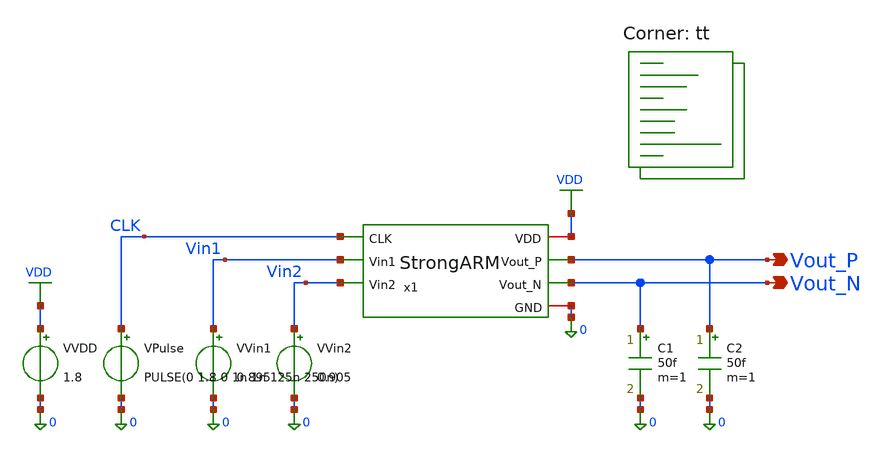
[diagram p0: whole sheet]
** sch_path: blocks/03_StrongARM/sim/tb_StrongARM_Power.sch
**.subckt tb_StrongARM_Power Vout_P Vout_N
*.opin Vout_P
*.opin Vout_N
x1 VDD CLK Vout_P Vout_N Vin1 Vin2 0 StrongARM
VVDD VDD 0 1.8
VVin1 Vin1 0 0.895
VVin2 Vin2 0 0.905
VPulse CLK 0 PULSE(0 1.8 0 1n 1n 125n 250n)
C1 Vout_N 0 50f m=1
C2 Vout_P 0 50f m=1
**** begin user architecture code



.control
save all

* ============================================
* BLOCK 3 - STRONGARM COMPARATOR
* TEST 7C - FINAL OUTPUT LOADING
* SKY130 TT / VDD 1.8V / CLK 4MHz
* BOTH INPUT POLARITIES
* ============================================

echo ============================================
echo TEST 7C - FINAL CHARACTERIZATION
echo ============================================

* ============================================
* CASE A: Vin1 < Vin2
* Vout_N should FALL
* Vout_P should remain HIGH
* ============================================

alter VVin1 0.895
alter VVin2 0.905

echo CASE A - NEGATIVE DIFFERENTIAL INPUT

tran 0.05n 2.5u

meas tran delay_A TRIG v(clk) VAL=0.9 RISE=9 TARG v(vout_n) VAL=0.9 FALL=9

meas tran vp_eval_A FIND v(vout_p) AT=2.01u
meas tran vn_eval_A FIND v(vout_n) AT=2.01u

meas tran vp_reset_A FIND v(vout_p) AT=2.20u
meas tran vn_reset_A FIND v(vout_n) AT=2.20u

meas tran vp_droop_A MIN v(vout_p) FROM=2u TO=2.01u

meas tran vp_max_A MAX v(vout_p) FROM=500n TO=2.5u
meas tran vn_max_A MAX v(vout_n) FROM=500n TO=2.5u

meas tran vp_min_A MIN v(vout_p) FROM=500n TO=2.5u
meas tran vn_min_A MIN v(vout_n) FROM=500n TO=2.5u

meas tran ivdd_A AVG i(VVDD) FROM=500n TO=2.5u

let power_A_uW = -1.8 * ivdd_A * 1e6
let energy_A_pJ = power_A_uW / 4
let delay_A_ns = delay_A * 1e9

echo CASE A SUMMARY
print power_A_uW
print energy_A_pJ
print delay_A_ns

* ============================================
* CASE B: Vin1 > Vin2
* Vout_P should FALL
* Vout_N should remain HIGH
* ============================================

alter VVin1 0.905
alter VVin2 0.895

echo CASE B - POSITIVE DIFFERENTIAL INPUT

tran 0.05n 2.5u

meas tran delay_B TRIG v(clk) VAL=0.9 RISE=9 TARG v(vout_p) VAL=0.9 FALL=9

meas tran vp_eval_B FIND v(vout_p) AT=2.01u
meas tran vn_eval_B FIND v(vout_n) AT=2.01u

meas tran vp_reset_B FIND v(vout_p) AT=2.20u
meas tran vn_reset_B FIND v(vout_n) AT=2.20u

meas tran vn_droop_B MIN v(vout_n) FROM=2u TO=2.01u

meas tran vp_max_B MAX v(vout_p) FROM=500n TO=2.5u
meas tran vn_max_B MAX v(vout_n) FROM=500n TO=2.5u

meas tran vp_min_B MIN v(vout_p) FROM=500n TO=2.5u
meas tran vn_min_B MIN v(vout_n) FROM=500n TO=2.5u

meas tran ivdd_B AVG i(VVDD) FROM=500n TO=2.5u

let power_B_uW = -1.8 * ivdd_B * 1e6
let energy_B_pJ = power_B_uW / 4
let delay_B_ns = delay_B * 1e9

echo CASE B SUMMARY
print power_B_uW
print energy_B_pJ
print delay_B_ns

echo ============================================
echo BOTH POLARITIES COMPLETED
echo ============================================

.endc

.lib $::SKYWATER_MODELS/sky130.lib.spice tt
**** end user architecture code
**.ends

* expanding   symbol:  blocks/03_StrongARM/xschem/StrongARM.sym # of pins=7
** sym_path: blocks/03_StrongARM/xschem/StrongARM.sym
** sch_path: blocks/03_StrongARM/xschem/StrongARM.sch
.subckt StrongARM VDD CLK Vout_P Vout_N Vin1 Vin2 GND
*.iopin VDD
*.iopin GND
*.ipin Vin1
*.ipin Vin2
*.ipin CLK
*.opin Vout_P
*.opin Vout_N
XS1 P CLK VDD VDD sky130_fd_pr__pfet_01v8 L=0.15 W=1.5 nf=1 ad='int((1 + 1)/2) * 1.5 / 1 * 0.29' as='int((1 + 2)/2) * 1.5 / 1 * 0.29'
+ pd='2*int((1 + 1)/2) * (1.5 / 1 + 0.29)' ps='2*int((1 + 2)/2) * (1.5 / 1 + 0.29)' nrd='0.29 / 1.5 ' nrs='0.29 / 1.5 '
+ sa=0 sb=0 sd=0 mult=1 m=1
XS3 Vout_P CLK VDD VDD sky130_fd_pr__pfet_01v8 L=0.15 W=1.5 nf=1 ad='int((1 + 1)/2) * 1.5 / 1 * 0.29'
+ as='int((1 + 2)/2) * 1.5 / 1 * 0.29' pd='2*int((1 + 1)/2) * (1.5 / 1 + 0.29)' ps='2*int((1 + 2)/2) * (1.5 / 1 + 0.29)'
+ nrd='0.29 / 1.5 ' nrs='0.29 / 1.5 ' sa=0 sb=0 sd=0 mult=1 m=1
XM5 Vout_P Vout_N VDD VDD sky130_fd_pr__pfet_01v8 L=0.3 W=5 nf=1 ad='int((1 + 1)/2) * 5 / 1 * 0.29' as='int((1 + 2)/2) * 5 / 1 * 0.29'
+ pd='2*int((1 + 1)/2) * (5 / 1 + 0.29)' ps='2*int((1 + 2)/2) * (5 / 1 + 0.29)' nrd='0.29 / 5 ' nrs='0.29 / 5 '
+ sa=0 sb=0 sd=0 mult=1 m=1
XM6 Vout_N Vout_P VDD VDD sky130_fd_pr__pfet_01v8 L=0.3 W=5 nf=1 ad='int((1 + 1)/2) * 5 / 1 * 0.29' as='int((1 + 2)/2) * 5 / 1 * 0.29'
+ pd='2*int((1 + 1)/2) * (5 / 1 + 0.29)' ps='2*int((1 + 2)/2) * (5 / 1 + 0.29)' nrd='0.29 / 5 ' nrs='0.29 / 5 '
+ sa=0 sb=0 sd=0 mult=1 m=1
XS4 Vout_N CLK VDD VDD sky130_fd_pr__pfet_01v8 L=0.15 W=1.5 nf=1 ad='int((1 + 1)/2) * 1.5 / 1 * 0.29'
+ as='int((1 + 2)/2) * 1.5 / 1 * 0.29' pd='2*int((1 + 1)/2) * (1.5 / 1 + 0.29)' ps='2*int((1 + 2)/2) * (1.5 / 1 + 0.29)'
+ nrd='0.29 / 1.5 ' nrs='0.29 / 1.5 ' sa=0 sb=0 sd=0 mult=1 m=1
XS2 Q CLK VDD VDD sky130_fd_pr__pfet_01v8 L=0.15 W=1.5 nf=1 ad='int((1 + 1)/2) * 1.5 / 1 * 0.29' as='int((1 + 2)/2) * 1.5 / 1 * 0.29'
+ pd='2*int((1 + 1)/2) * (1.5 / 1 + 0.29)' ps='2*int((1 + 2)/2) * (1.5 / 1 + 0.29)' nrd='0.29 / 1.5 ' nrs='0.29 / 1.5 '
+ sa=0 sb=0 sd=0 mult=1 m=1
XM3 Vout_P Vout_N P GND sky130_fd_pr__nfet_01v8 L=0.3 W=2 nf=1 ad='int((1 + 1)/2) * 2 / 1 * 0.29' as='int((1 + 2)/2) * 2 / 1 * 0.29'
+ pd='2*int((1 + 1)/2) * (2 / 1 + 0.29)' ps='2*int((1 + 2)/2) * (2 / 1 + 0.29)' nrd='0.29 / 2 ' nrs='0.29 / 2 '
+ sa=0 sb=0 sd=0 mult=1 m=1
XM4 Vout_N Vout_P Q GND sky130_fd_pr__nfet_01v8 L=0.3 W=2 nf=1 ad='int((1 + 1)/2) * 2 / 1 * 0.29' as='int((1 + 2)/2) * 2 / 1 * 0.29'
+ pd='2*int((1 + 1)/2) * (2 / 1 + 0.29)' ps='2*int((1 + 2)/2) * (2 / 1 + 0.29)' nrd='0.29 / 2 ' nrs='0.29 / 2 '
+ sa=0 sb=0 sd=0 mult=1 m=1
XM1 P Vin1 TAIL GND sky130_fd_pr__nfet_01v8 L=0.5 W=10 nf=1 ad='int((1 + 1)/2) * 10 / 1 * 0.29' as='int((1 + 2)/2) * 10 / 1 * 0.29'
+ pd='2*int((1 + 1)/2) * (10 / 1 + 0.29)' ps='2*int((1 + 2)/2) * (10 / 1 + 0.29)' nrd='0.29 / 10 ' nrs='0.29 / 10 '
+ sa=0 sb=0 sd=0 mult=1 m=1
XM2 Q Vin2 TAIL GND sky130_fd_pr__nfet_01v8 L=0.5 W=10 nf=1 ad='int((1 + 1)/2) * 10 / 1 * 0.29' as='int((1 + 2)/2) * 10 / 1 * 0.29'
+ pd='2*int((1 + 1)/2) * (10 / 1 + 0.29)' ps='2*int((1 + 2)/2) * (10 / 1 + 0.29)' nrd='0.29 / 10 ' nrs='0.29 / 10 '
+ sa=0 sb=0 sd=0 mult=1 m=1
XM7 TAIL CLK GND GND sky130_fd_pr__nfet_01v8 L=0.3 W=1 nf=1 ad='int((1 + 1)/2) * 1 / 1 * 0.29' as='int((1 + 2)/2) * 1 / 1 * 0.29'
+ pd='2*int((1 + 1)/2) * (1 / 1 + 0.29)' ps='2*int((1 + 2)/2) * (1 / 1 + 0.29)' nrd='0.29 / 1 ' nrs='0.29 / 1 '
+ sa=0 sb=0 sd=0 mult=1 m=1
.ends

.GLOBAL VDD
.end
